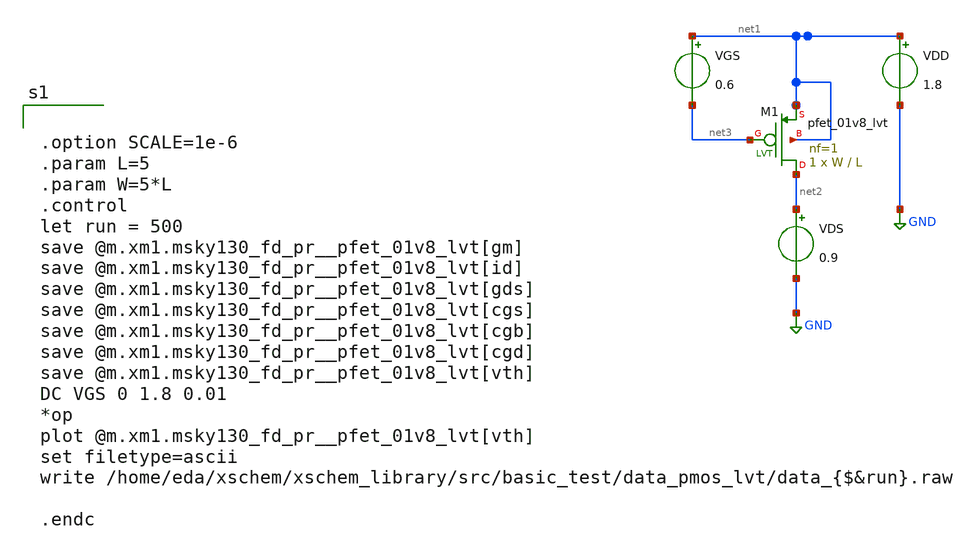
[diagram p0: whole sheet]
** sch_path: xschem/src/basic_test/gm_id_pmos.sch
**.subckt gm_id_pmos
VDD net1 GND 1.8
XM1 net2 net3 net1 net1 sky130_fd_pr__pfet_01v8_lvt L=L W=W nf=1 ad='int((nf+1)/2) * W/nf * 0.29' as='int((nf+2)/2) * W/nf * 0.29'
+ pd='2*int((nf+1)/2) * (W/nf + 0.29)' ps='2*int((nf+2)/2) * (W/nf + 0.29)' nrd='0.29 / W' nrs='0.29 / W'
+ sa=0 sb=0 sd=0 mult=1 m=1
VGS net1 net3 0.6
VDS net2 GND 0.9
**** begin user architecture code


.include $::SKYWATER_MODELS/cells/nfet_01v8/sky130_fd_pr__nfet_01v8__tt.corner.spice
.include $::SKYWATER_MODELS/cells/nfet_01v8_lvt/sky130_fd_pr__nfet_01v8_lvt__tt.corner.spice
.include $::SKYWATER_MODELS/cells/pfet_01v8/sky130_fd_pr__pfet_01v8__tt.corner.spice
.include $::SKYWATER_MODELS/cells/nfet_03v3_nvt/sky130_fd_pr__nfet_03v3_nvt__tt.corner.spice
.include $::SKYWATER_MODELS/cells/nfet_05v0_nvt/sky130_fd_pr__nfet_05v0_nvt__tt.corner.spice
.include $::SKYWATER_MODELS/cells/esd_nfet_01v8/sky130_fd_pr__esd_nfet_01v8__tt.corner.spice
.include $::SKYWATER_MODELS/cells/pfet_01v8_lvt/sky130_fd_pr__pfet_01v8_lvt__tt.corner.spice
.include $::SKYWATER_MODELS/cells/pfet_01v8_hvt/sky130_fd_pr__pfet_01v8_hvt__tt.corner.spice
.include $::SKYWATER_MODELS/cells/esd_pfet_g5v0d10v5/sky130_fd_pr__esd_pfet_g5v0d10v5__tt.corner.spice
.include $::SKYWATER_MODELS/cells/pfet_g5v0d10v5/sky130_fd_pr__pfet_g5v0d10v5__tt.corner.spice
.include $::SKYWATER_MODELS/cells/pfet_g5v0d16v0/sky130_fd_pr__pfet_g5v0d16v0__tt.corner.spice
.include $::SKYWATER_MODELS/cells/nfet_g5v0d10v5/sky130_fd_pr__nfet_g5v0d10v5__tt.corner.spice
.include $::SKYWATER_MODELS/cells/nfet_g5v0d16v0/sky130_fd_pr__nfet_g5v0d16v0__tt_discrete.corner.spice
.include $::SKYWATER_MODELS/cells/esd_nfet_g5v0d10v5/sky130_fd_pr__esd_nfet_g5v0d10v5__tt.corner.spice
.include $::SKYWATER_MODELS/models/corners/tt/nonfet.spice
* Mismatch parameters
.include $::SKYWATER_MODELS/cells/nfet_01v8/sky130_fd_pr__nfet_01v8__mismatch.corner.spice
.include $::SKYWATER_MODELS/cells/pfet_01v8/sky130_fd_pr__pfet_01v8__mismatch.corner.spice
.include $::SKYWATER_MODELS/cells/nfet_01v8_lvt/sky130_fd_pr__nfet_01v8_lvt__mismatch.corner.spice
.include $::SKYWATER_MODELS/cells/pfet_01v8_lvt/sky130_fd_pr__pfet_01v8_lvt__mismatch.corner.spice
.include $::SKYWATER_MODELS/cells/pfet_01v8_hvt/sky130_fd_pr__pfet_01v8_hvt__mismatch.corner.spice
.include $::SKYWATER_MODELS/cells/nfet_g5v0d10v5/sky130_fd_pr__nfet_g5v0d10v5__mismatch.corner.spice
.include $::SKYWATER_MODELS/cells/pfet_g5v0d10v5/sky130_fd_pr__pfet_g5v0d10v5__mismatch.corner.spice
.include $::SKYWATER_MODELS/cells/nfet_05v0_nvt/sky130_fd_pr__nfet_05v0_nvt__mismatch.corner.spice
.include $::SKYWATER_MODELS/cells/nfet_03v3_nvt/sky130_fd_pr__nfet_03v3_nvt__mismatch.corner.spice
* Resistor$::SKYWATER_MODELS/Capacitor
.include $::SKYWATER_MODELS/models/r+c/res_typical__cap_typical.spice
.include $::SKYWATER_MODELS/models/r+c/res_typical__cap_typical__lin.spice
* Special cells
.include $::SKYWATER_MODELS/models/corners/tt/specialized_cells.spice
* All models
.include $::SKYWATER_MODELS/models/all.spice
* Corner
.include $::SKYWATER_MODELS/models/corners/tt/rf.spice



.option SCALE=1e-6
.param L=5
.param W=5*L
.control
let run = 500
save @m.xm1.msky130_fd_pr__pfet_01v8_lvt[gm]
save @m.xm1.msky130_fd_pr__pfet_01v8_lvt[id]
save @m.xm1.msky130_fd_pr__pfet_01v8_lvt[gds]
save @m.xm1.msky130_fd_pr__pfet_01v8_lvt[cgs]
save @m.xm1.msky130_fd_pr__pfet_01v8_lvt[cgb]
save @m.xm1.msky130_fd_pr__pfet_01v8_lvt[cgd]
save @m.xm1.msky130_fd_pr__pfet_01v8_lvt[vth]
DC VGS 0 1.8 0.01
*op
plot @m.xm1.msky130_fd_pr__pfet_01v8_lvt[vth]
set filetype=ascii
write /home/eda/xschem/xschem_library/src/basic_test/data_pmos_lvt/data_{$&run}.raw

.endc


**** end user architecture code
**.ends
.GLOBAL GND
.end
